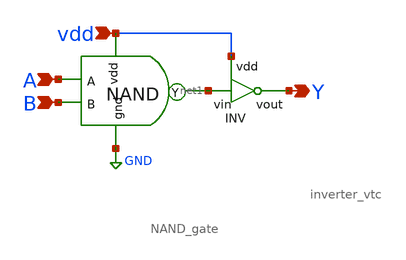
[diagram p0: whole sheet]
** sch_path: Circuit Files/Logic gate design using MOSFETS/gates/AND_gate.sch
**.subckt AND_gate Y A B vdd
*.opin Y
*.ipin A
*.ipin B
*.ipin vdd
x1 vdd net1 A B GND NAND_gate
x2 vdd net1 Y inverter_vtc
**.ends

* expanding   symbol:  daVLSI_World/gates/NAND_gate.sym # of pins=5
** sym_path: Circuit Files/Logic gate design using MOSFETS/gates/NAND_gate.sym
** sch_path: Circuit Files/Logic gate design using MOSFETS/gates/NAND_gate.sch
.subckt NAND_gate vdd Y A B gnd
*.ipin A
*.ipin B
*.opin Y
*.ipin vdd
*.ipin gnd
XM1 Y A net1 gnd sky130_fd_pr__nfet_01v8 L=0.15 W=1 nf=1 ad='int((nf+1)/2) * W/nf * 0.29' as='int((nf+2)/2) * W/nf * 0.29'
+ pd='2*int((nf+1)/2) * (W/nf + 0.29)' ps='2*int((nf+2)/2) * (W/nf + 0.29)' nrd='0.29 / W' nrs='0.29 / W'
+ sa=0 sb=0 sd=0 mult=1 m=1
XM2 net1 B gnd gnd sky130_fd_pr__nfet_01v8 L=0.15 W=1 nf=1 ad='int((nf+1)/2) * W/nf * 0.29' as='int((nf+2)/2) * W/nf * 0.29'
+ pd='2*int((nf+1)/2) * (W/nf + 0.29)' ps='2*int((nf+2)/2) * (W/nf + 0.29)' nrd='0.29 / W' nrs='0.29 / W'
+ sa=0 sb=0 sd=0 mult=1 m=1
XM3 Y A vdd vdd sky130_fd_pr__pfet_01v8 L=0.15 W=2 nf=1 ad='int((nf+1)/2) * W/nf * 0.29' as='int((nf+2)/2) * W/nf * 0.29'
+ pd='2*int((nf+1)/2) * (W/nf + 0.29)' ps='2*int((nf+2)/2) * (W/nf + 0.29)' nrd='0.29 / W' nrs='0.29 / W'
+ sa=0 sb=0 sd=0 mult=1 m=1
XM4 Y B vdd vdd sky130_fd_pr__pfet_01v8 L=0.15 W=2 nf=1 ad='int((nf+1)/2) * W/nf * 0.29' as='int((nf+2)/2) * W/nf * 0.29'
+ pd='2*int((nf+1)/2) * (W/nf + 0.29)' ps='2*int((nf+2)/2) * (W/nf + 0.29)' nrd='0.29 / W' nrs='0.29 / W'
+ sa=0 sb=0 sd=0 mult=1 m=1
.ends


* expanding   symbol:  daVLSI_World/gates/inverter_vtc.sym # of pins=3
** sym_path: Circuit Files/Logic gate design using MOSFETS/gates/inverter_vtc.sym
** sch_path: Circuit Files/Logic gate design using MOSFETS/gates/inverter_vtc.sch
.subckt inverter_vtc vdd vin vout
*.ipin vin
*.opin vout
*.ipin vdd
XM1 vout vin GND GND sky130_fd_pr__nfet_01v8 L=0.15 W=1 nf=1 ad='int((nf+1)/2) * W/nf * 0.29' as='int((nf+2)/2) * W/nf * 0.29'
+ pd='2*int((nf+1)/2) * (W/nf + 0.29)' ps='2*int((nf+2)/2) * (W/nf + 0.29)' nrd='0.29 / W' nrs='0.29 / W'
+ sa=0 sb=0 sd=0 mult=1 m=1
XM2 vout vin vdd vdd sky130_fd_pr__pfet_01v8 L=0.15 W=2 nf=1 ad='int((nf+1)/2) * W/nf * 0.29' as='int((nf+2)/2) * W/nf * 0.29'
+ pd='2*int((nf+1)/2) * (W/nf + 0.29)' ps='2*int((nf+2)/2) * (W/nf + 0.29)' nrd='0.29 / W' nrs='0.29 / W'
+ sa=0 sb=0 sd=0 mult=1 m=1
.ends

.GLOBAL GND
.end
